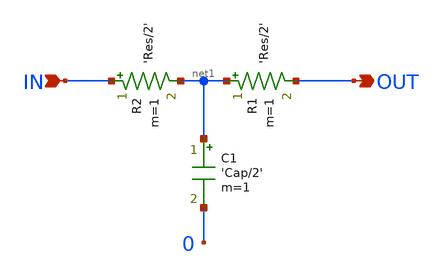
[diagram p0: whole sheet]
** sch_path: xschem-src/xschem_library/examples/rcline.sch
* Copyright (C) 1998-2026 Stefan Frederik Schippers
* This program is free software; you can redistribute it and/or modify
* it under the terms of the GNU General Public License as published by
* the Free Software Foundation; either version 2 of the License, or
* (at your option) any later version.
* This program is distributed in the hope that it will be useful,
* but WITHOUT ANY WARRANTY; without even the implied warranty of
* MERCHANTABILITY or FITNESS FOR A PARTICULAR PURPOSE.  See the
* GNU General Public License for more details.
* You should have received a copy of the GNU General Public License
* along with this program; if not, write to the Free Software
**.subckt rcline IN OUT
*.ipin IN
*.opin OUT
C1 net1 0 'Cap/2' m=1
R1 net1 OUT 'Res/2' m=1
R2 IN net1 'Res/2' m=1
**.ends
.end
